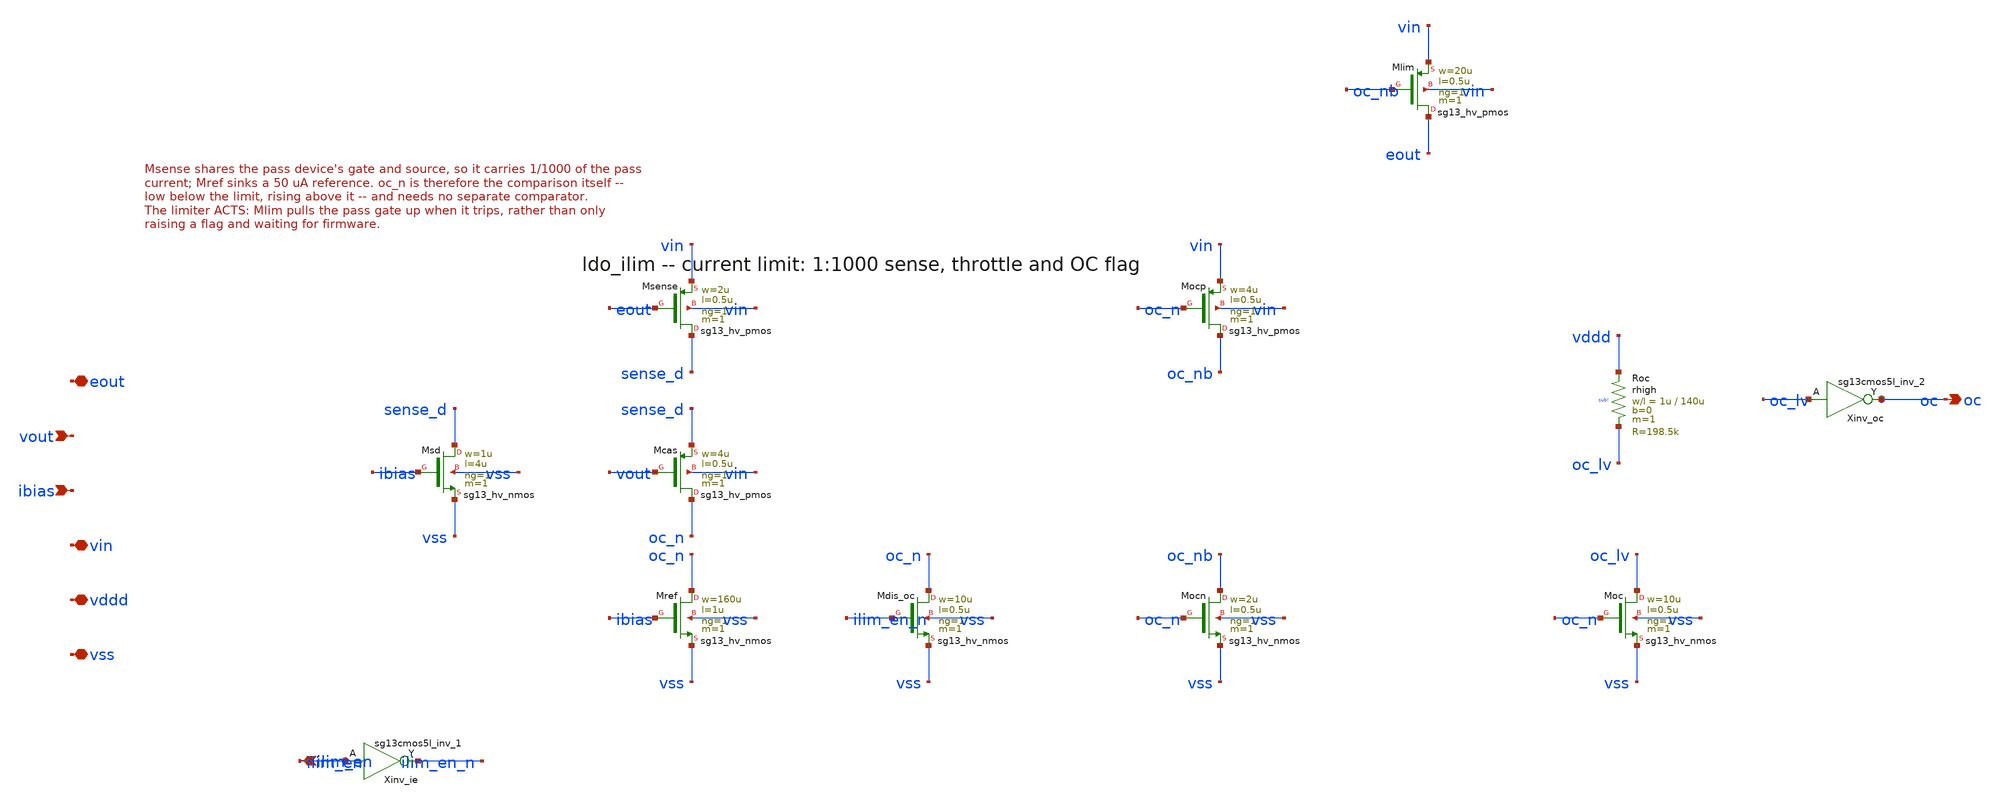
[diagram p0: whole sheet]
** sch_path: xschem/ldo_ilim.sch
**.subckt ldo_ilim eout vout ibias ilim_en oc vin vddd vss
*.iopin eout
*.ipin vout
*.ipin ibias
*.ipin ilim_en
*.opin oc
*.iopin vin
*.iopin vddd
*.iopin vss
XMsense sense_d eout vin vin sg13_hv_pmos w=2u l=0.5u ng=1 m=1 mm_ok=1
XMsd sense_d ibias vss vss sg13_hv_nmos w=1u l=4u ng=1 m=1 mm_ok=1
XMcas oc_n vout sense_d vin sg13_hv_pmos w=4u l=0.5u ng=1 m=1 mm_ok=1
XMref oc_n ibias vss vss sg13_hv_nmos w=160u l=1u ng=1 m=1 mm_ok=1
XMdis_oc oc_n ilim_en_n vss vss sg13_hv_nmos w=10u l=0.5u ng=1 m=1 mm_ok=1
Xinv_ie ilim_en_n ilim_en vddd vss sg13cmos5l_inv_1
XMocp oc_nb oc_n vin vin sg13_hv_pmos w=4u l=0.5u ng=1 m=1 mm_ok=1
XMocn oc_nb oc_n vss vss sg13_hv_nmos w=2u l=0.5u ng=1 m=1 mm_ok=1
XMlim eout oc_nb vin vin sg13_hv_pmos w=20u l=0.5u ng=1 m=1 mm_ok=1
XRoc vddd oc_lv sub! rhigh w=1u l=140u m=1 b=0 mm_ok=1
XMoc oc_lv oc_n vss vss sg13_hv_nmos w=10u l=0.5u ng=1 m=1 mm_ok=1
Xinv_oc oc oc_lv vddd vss sg13cmos5l_inv_2
**.ends
.end
